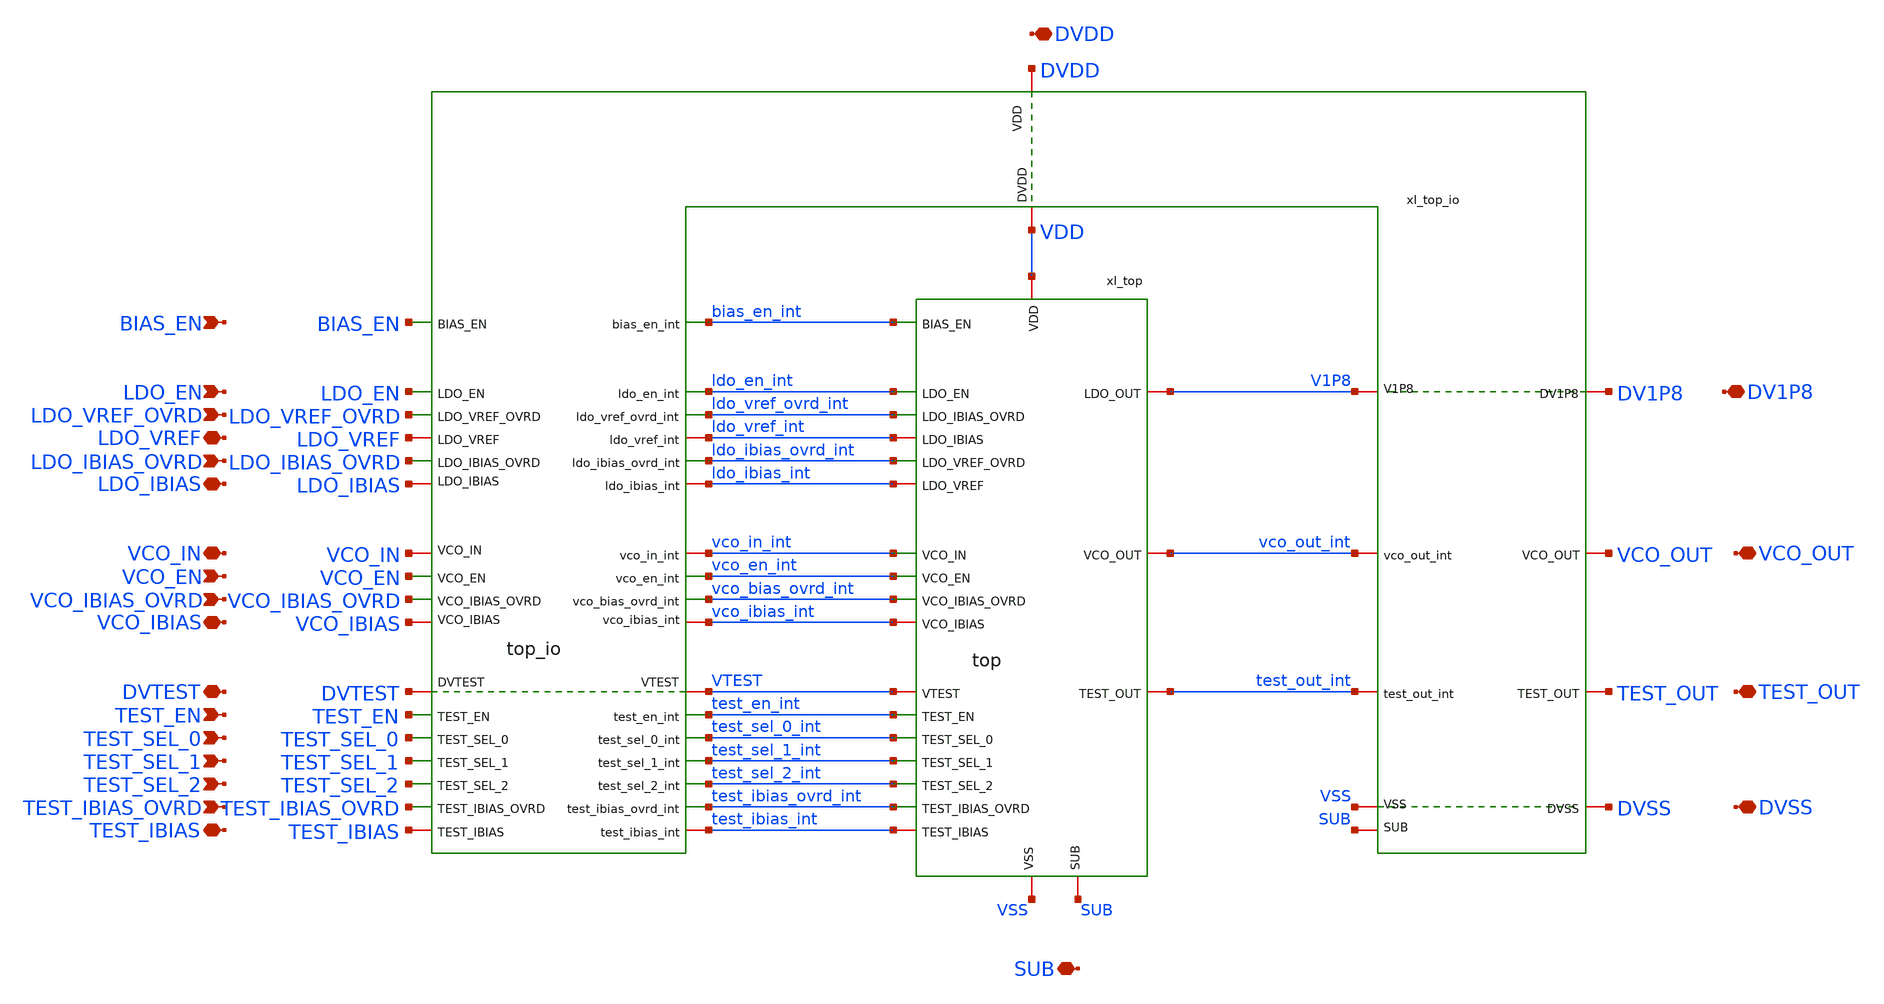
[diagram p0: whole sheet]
** sch_path: designs/libs/A_track_core/chiptop_A_track/chiptop_A_track.sch
**.subckt chiptop_A_track VCO_OUT VCO_IN VCO_IBIAS_OVRD VCO_IBIAS VCO_EN TEST_SEL_2 TEST_SEL_1
*+ TEST_SEL_0 TEST_OUT TEST_IBIAS_OVRD TEST_IBIAS TEST_EN SUB LDO_VREF_OVRD LDO_VREF LDO_IBIAS_OVRD LDO_IBIAS
*+ LDO_EN DVTEST DVSS DVDD DV1P8 BIAS_EN
*.iopin VCO_OUT
*.iopin VCO_IN
*.ipin VCO_IBIAS_OVRD
*.iopin VCO_IBIAS
*.ipin VCO_EN
*.ipin TEST_SEL_2
*.ipin TEST_SEL_1
*.ipin TEST_SEL_0
*.iopin TEST_OUT
*.ipin TEST_IBIAS_OVRD
*.iopin TEST_IBIAS
*.ipin TEST_EN
*.iopin SUB
*.ipin LDO_VREF_OVRD
*.iopin LDO_VREF
*.ipin LDO_IBIAS_OVRD
*.iopin LDO_IBIAS
*.ipin LDO_EN
*.iopin DVTEST
*.iopin DVSS
*.iopin DVDD
*.iopin DV1P8
*.ipin BIAS_EN
xI_top VDD vco_in_int V1P8 vco_out_int vco_en_int test_out_int test_en_int test_sel_0_int SUB VSS
+ vco_bias_ovrd_int vco_ibias_int test_ibias_ovrd_int test_ibias_int ldo_en_int ldo_vref_ovrd_int ldo_vref_int
+ ldo_ibias_ovrd_int ldo_ibias_int test_sel_1_int test_sel_2_int VTEST bias_en_int top
xI_top_io VDD DVDD bias_en_int BIAS_EN ldo_en_int LDO_EN ldo_vref_ovrd_int LDO_VREF_OVRD
+ ldo_vref_int LDO_VREF DV1P8 V1P8 LDO_IBIAS_OVRD ldo_ibias_ovrd_int LDO_IBIAS ldo_ibias_int VCO_IN vco_in_int
+ vco_en_int VCO_EN VCO_OUT vco_out_int vco_bias_ovrd_int VCO_IBIAS_OVRD VCO_IBIAS DVTEST VTEST test_out_int
+ TEST_OUT test_en_int TEST_EN test_sel_0_int TEST_SEL_0 TEST_SEL_1 test_sel_1_int TEST_SEL_2 test_sel_2_int
+ test_ibias_ovrd_int TEST_IBIAS_OVRD test_ibias_int TEST_IBIAS DVSS SUB VSS vco_ibias_int top_io
**.ends
.end
